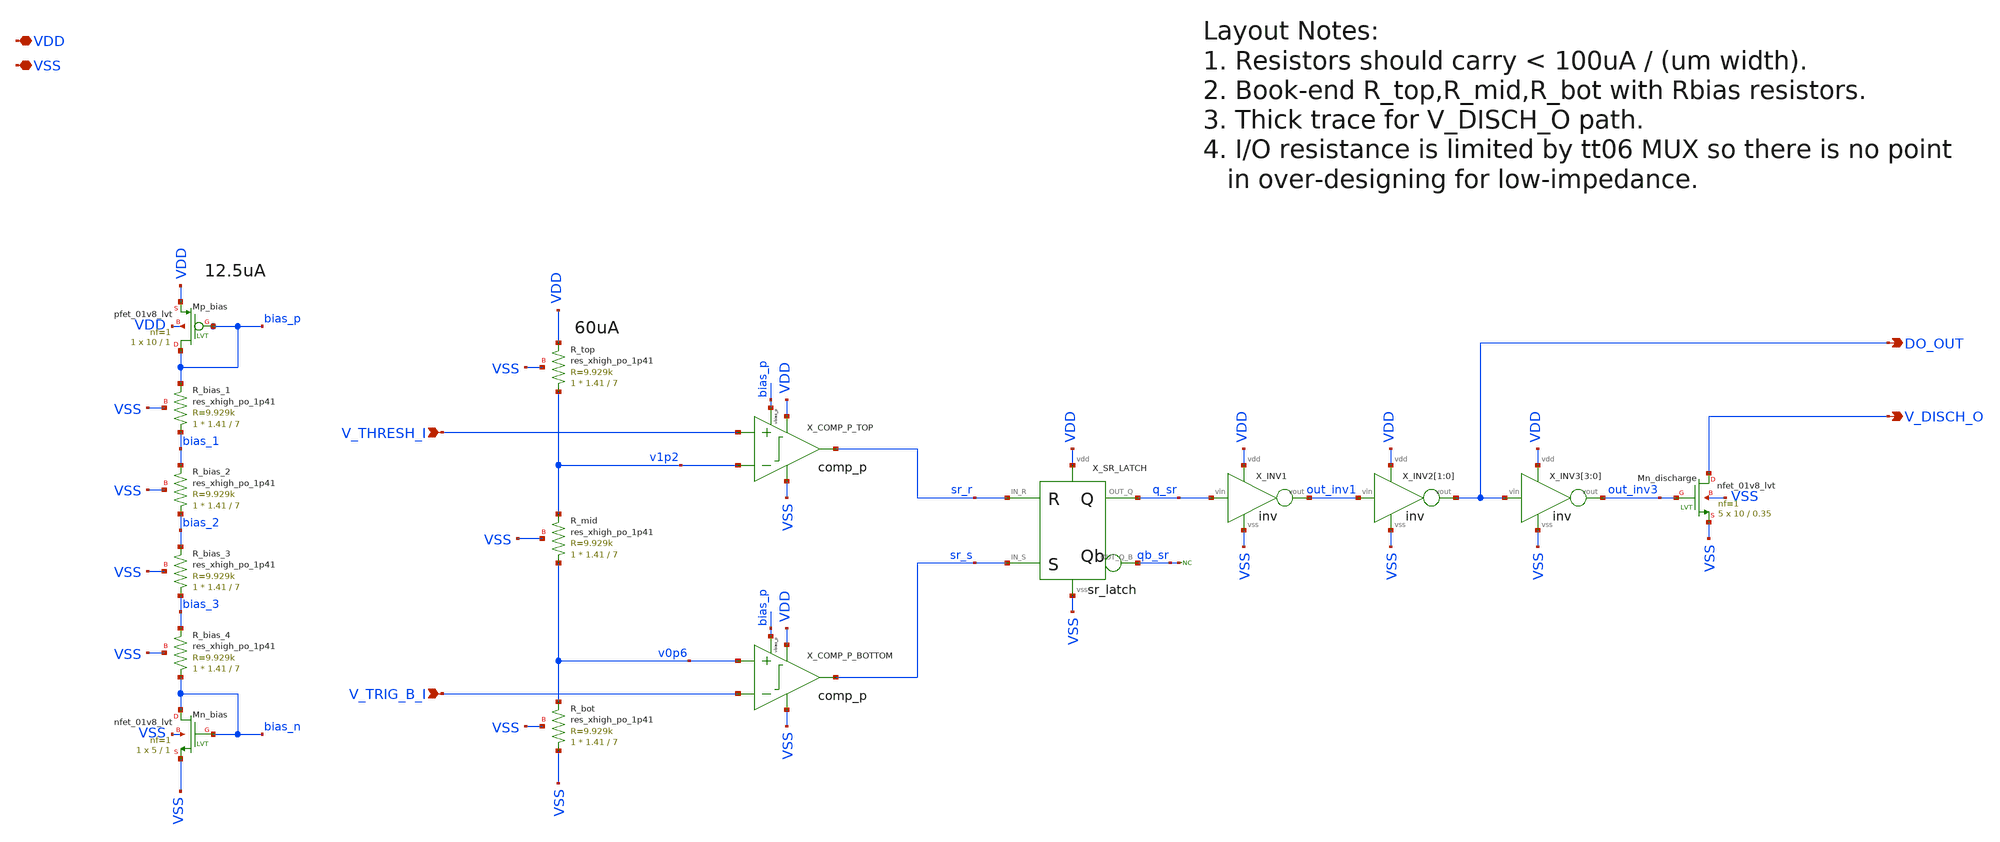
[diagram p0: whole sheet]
** sch_path: xsch/ip/timers/timer_core/timer_core.sch
**.subckt timer_core V_THRESH_I V_TRIG_B_I DO_OUT VDD VSS V_DISCH_O
*.ipin V_THRESH_I
*.ipin V_TRIG_B_I
*.opin DO_OUT
*.iopin VDD
*.iopin VSS
*.opin V_DISCH_O
XR_top v1p2 VDD VSS sky130_fd_pr__res_xhigh_po_1p41 L=7 mult=1 m=1
XR_mid v0p6 v1p2 VSS sky130_fd_pr__res_xhigh_po_1p41 L=7 mult=1 m=1
XR_bot VSS v0p6 VSS sky130_fd_pr__res_xhigh_po_1p41 L=7 mult=1 m=1
* noconn qb_sr
XR_bias_1 bias_1 bias_p VSS sky130_fd_pr__res_xhigh_po_1p41 L=7 mult=1 m=1
XMn_bias bias_n bias_n VSS VSS sky130_fd_pr__nfet_01v8_lvt L=1 W=5 nf=1 ad='int((nf+1)/2) * W/nf * 0.29'
+ as='int((nf+2)/2) * W/nf * 0.29' pd='2*int((nf+1)/2) * (W/nf + 0.29)' ps='2*int((nf+2)/2) * (W/nf + 0.29)'
+ nrd='0.29 / W' nrs='0.29 / W' sa=0 sb=0 sd=0 mult=1 m=1
XMp_bias bias_p bias_p VDD VDD sky130_fd_pr__pfet_01v8_lvt L=1 W=10 nf=1 ad='int((nf+1)/2) * W/nf * 0.29'
+ as='int((nf+2)/2) * W/nf * 0.29' pd='2*int((nf+1)/2) * (W/nf + 0.29)' ps='2*int((nf+2)/2) * (W/nf + 0.29)'
+ nrd='0.29 / W' nrs='0.29 / W' sa=0 sb=0 sd=0 mult=1 m=1
XMn_discharge V_DISCH_O out_inv3 VSS VSS sky130_fd_pr__nfet_01v8_lvt L=0.35 W=10 nf=1 ad='int((nf+1)/2) * W/nf * 0.29'
+ as='int((nf+2)/2) * W/nf * 0.29' pd='2*int((nf+1)/2) * (W/nf + 0.29)' ps='2*int((nf+2)/2) * (W/nf + 0.29)'
+ nrd='0.29 / W' nrs='0.29 / W' sa=0 sb=0 sd=0 mult=5 m=5
XR_bias_2 bias_2 bias_1 VSS sky130_fd_pr__res_xhigh_po_1p41 L=7 mult=1 m=1
XR_bias_3 bias_3 bias_2 VSS sky130_fd_pr__res_xhigh_po_1p41 L=7 mult=1 m=1
XR_bias_4 bias_n bias_3 VSS sky130_fd_pr__res_xhigh_po_1p41 L=7 mult=1 m=1
X_INV3[3] DO_OUT out_inv3 VDD VSS inv
X_INV3[2] DO_OUT out_inv3 VDD VSS inv
X_INV3[1] DO_OUT out_inv3 VDD VSS inv
X_INV3[0] DO_OUT out_inv3 VDD VSS inv
X_INV2[1] out_inv1 DO_OUT VDD VSS inv
X_INV2[0] out_inv1 DO_OUT VDD VSS inv
X_INV1 q_sr out_inv1 VDD VSS inv
X_SR_LATCH sr_s sr_r q_sr qb_sr VDD VSS sr_latch
X_COMP_P_BOTTOM v0p6 V_TRIG_B_I bias_p sr_s VDD VSS comp_p
X_COMP_P_TOP V_THRESH_I v1p2 bias_p sr_r VDD VSS comp_p
**.ends
.end
